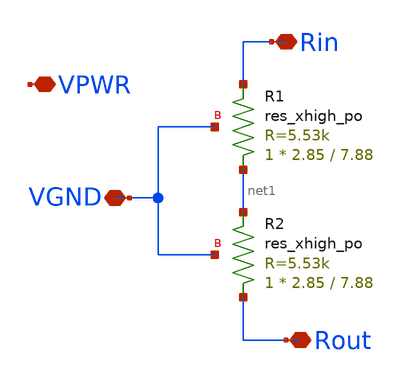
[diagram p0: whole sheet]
** sch_path: xschem/xschem/skywater_asc_res_xhigh_po_2p85_1.sch
**.subckt skywater_asc_res_xhigh_po_2p85_1 Rin Rout VPWR VGND
*.iopin Rin
*.iopin Rout
*.iopin VPWR
*.iopin VGND
XR1 net1 Rin VGND sky130_fd_pr__res_xhigh_po W=2.85 L=7.88 mult=1 m=1
XR2 Rout net1 VGND sky130_fd_pr__res_xhigh_po W=2.85 L=7.88 mult=1 m=1
**.ends
.end
